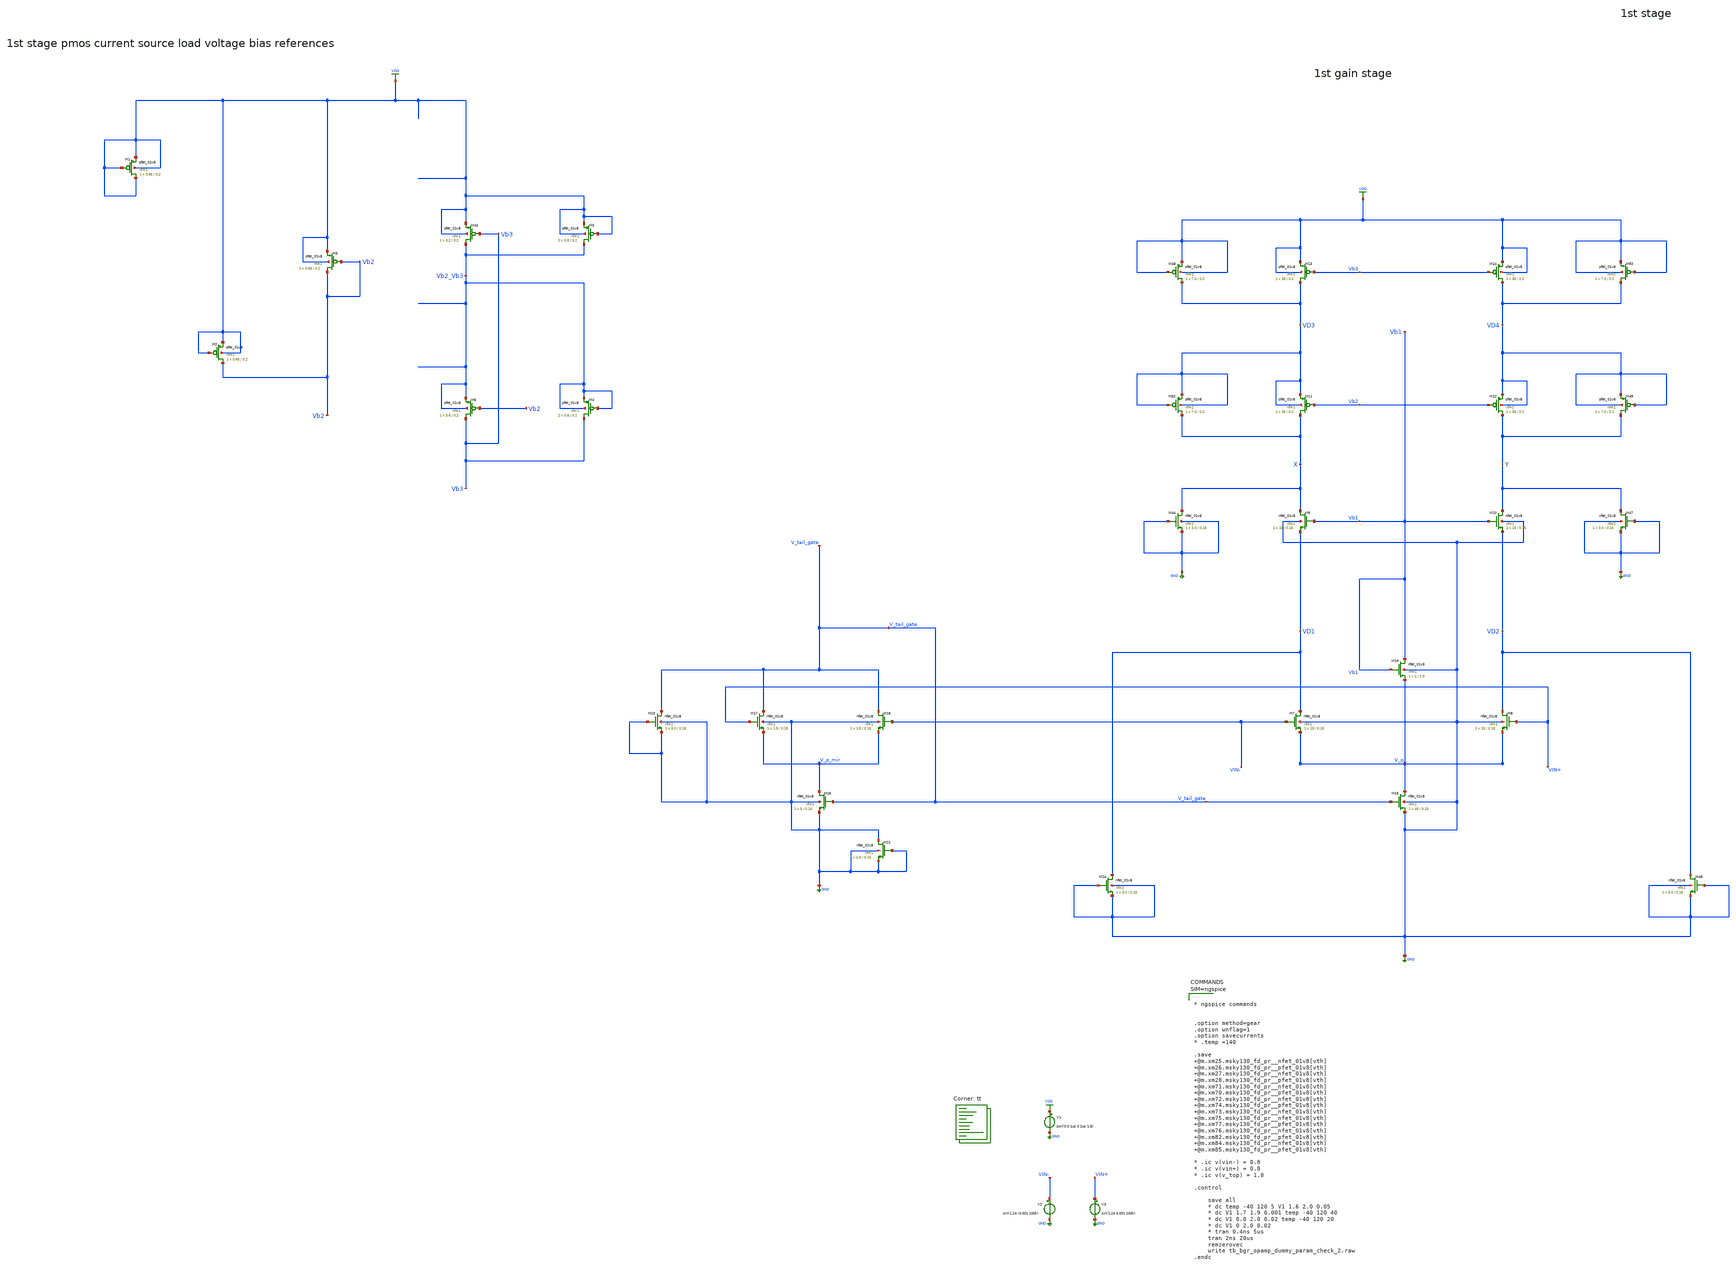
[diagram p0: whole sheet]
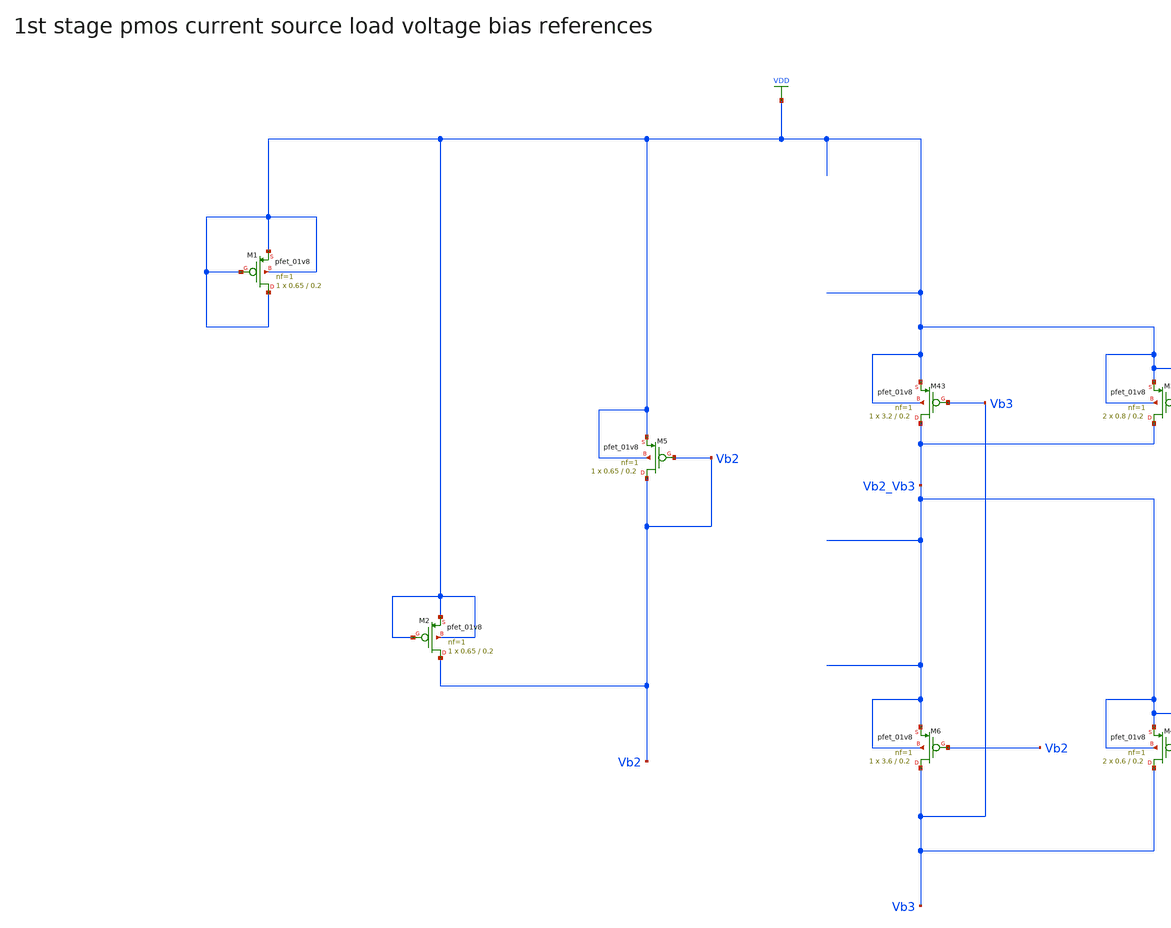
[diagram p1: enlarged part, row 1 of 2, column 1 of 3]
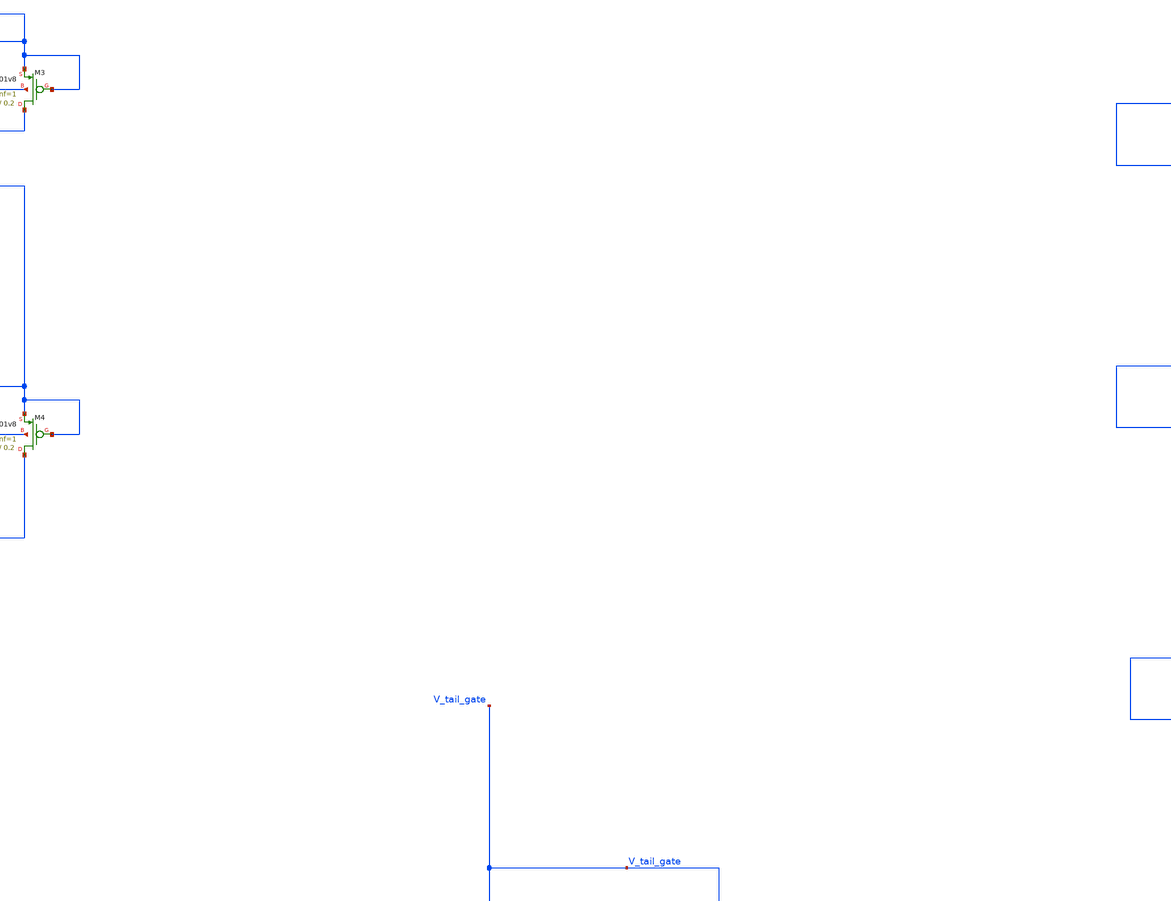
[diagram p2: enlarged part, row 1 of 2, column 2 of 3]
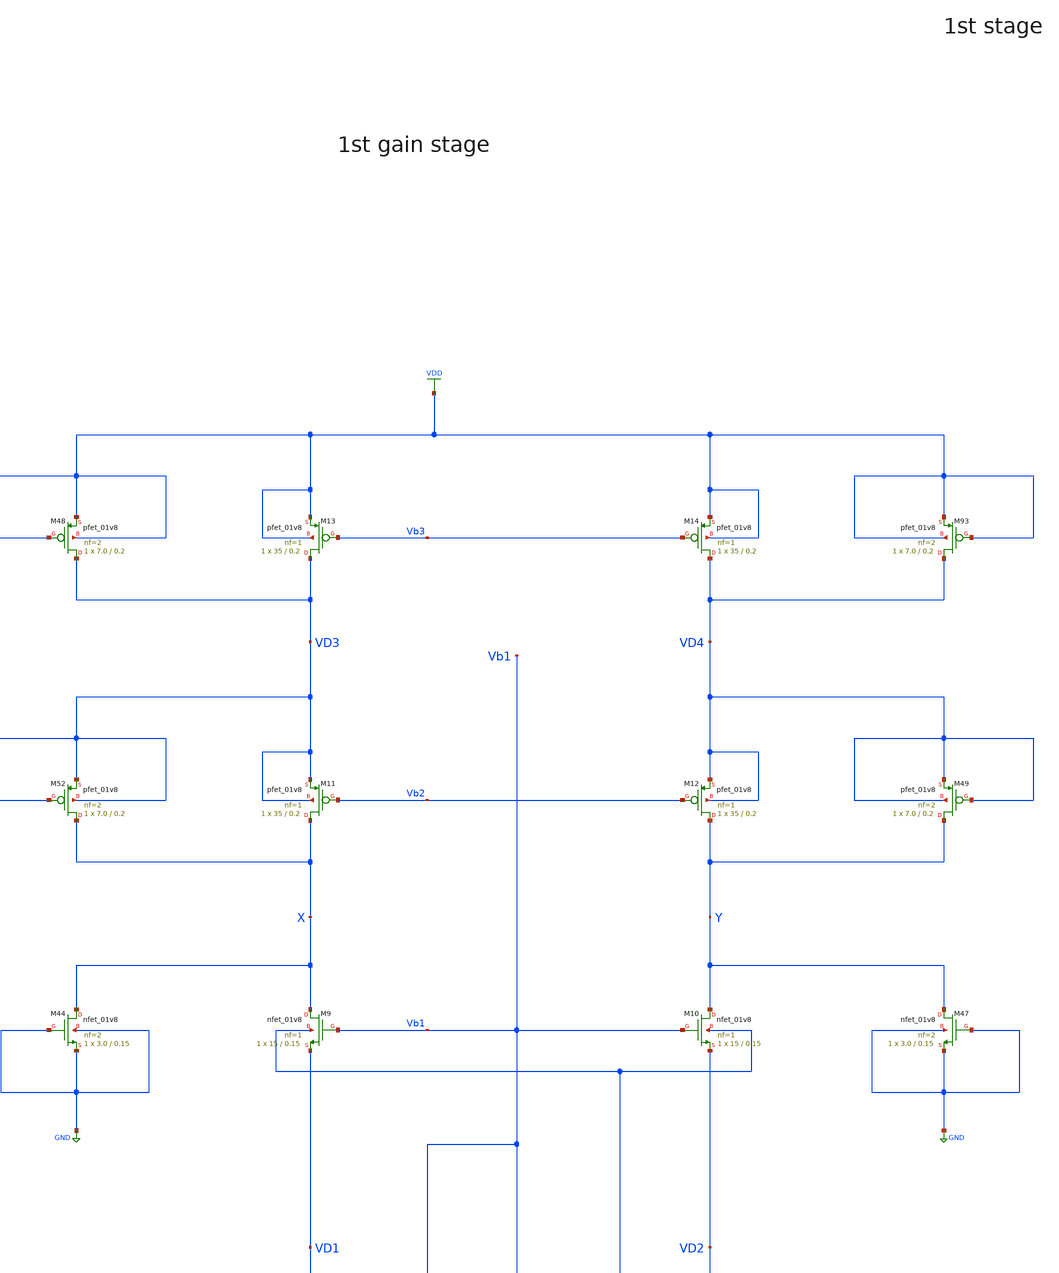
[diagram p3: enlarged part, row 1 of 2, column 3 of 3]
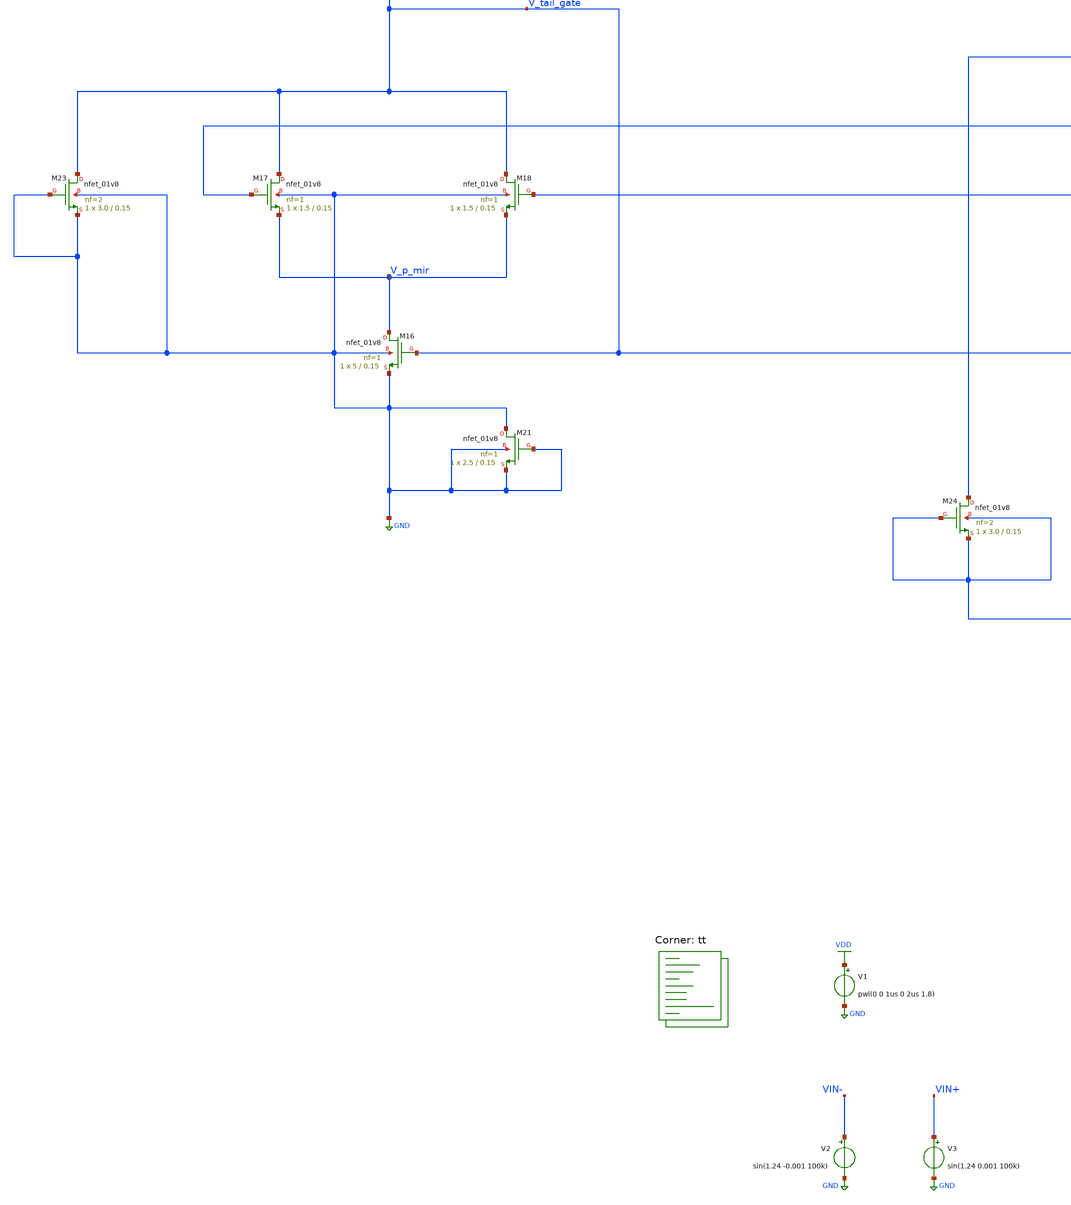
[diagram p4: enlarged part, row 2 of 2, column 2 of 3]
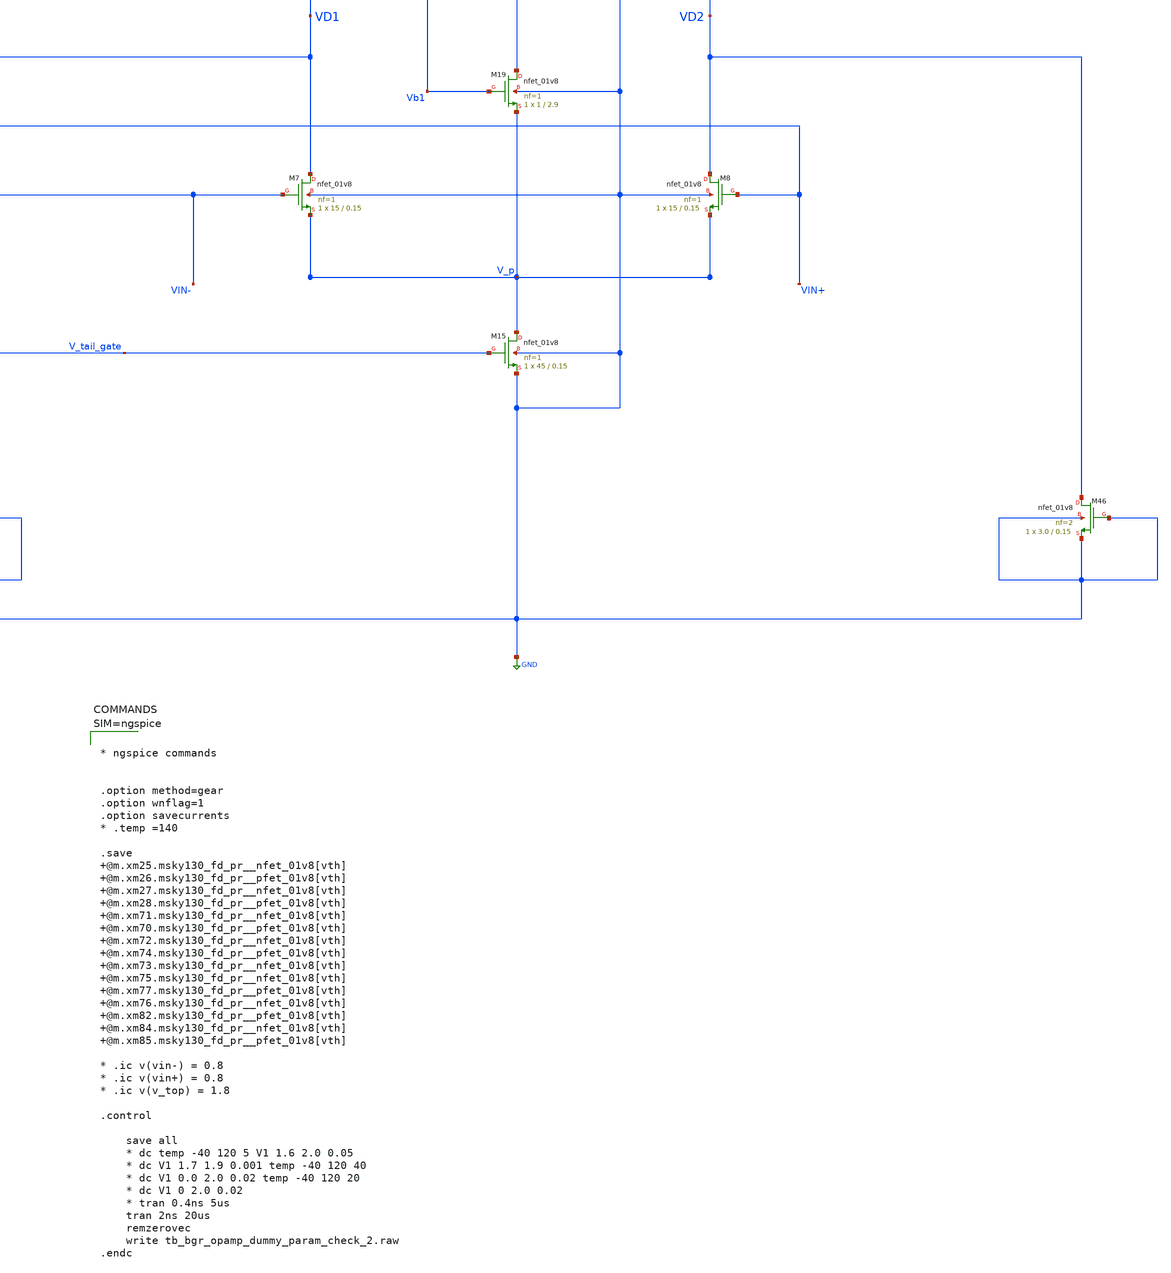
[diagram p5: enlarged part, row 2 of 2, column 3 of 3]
** sch_path: projects/ASU/EEE572/schematic/tb_bgr_opamp_dummy_param_check_2.sch
**.subckt tb_bgr_opamp_dummy_param_check_2
V1 VDD GND pwl(0 0 1us 0 2us 1.8)
XM7 VD1 VIN- V_p GND sky130_fd_pr__nfet_01v8 L=0.15 W=15 nf=1 ad='int((nf+1)/2) * W/nf * 0.29' as='int((nf+2)/2) * W/nf * 0.29'
+ pd='2*int((nf+1)/2) * (W/nf + 0.29)' ps='2*int((nf+2)/2) * (W/nf + 0.29)' nrd='0.29 / W' nrs='0.29 / W'
+ sa=0 sb=0 sd=0 mult=1 m=1
XM8 VD2 VIN+ V_p GND sky130_fd_pr__nfet_01v8 L=0.15 W=15 nf=1 ad='int((nf+1)/2) * W/nf * 0.29' as='int((nf+2)/2) * W/nf * 0.29'
+ pd='2*int((nf+1)/2) * (W/nf + 0.29)' ps='2*int((nf+2)/2) * (W/nf + 0.29)' nrd='0.29 / W' nrs='0.29 / W'
+ sa=0 sb=0 sd=0 mult=1 m=1
XM9 X Vb1 VD1 GND sky130_fd_pr__nfet_01v8 L=0.15 W=15 nf=1 ad='int((nf+1)/2) * W/nf * 0.29' as='int((nf+2)/2) * W/nf * 0.29'
+ pd='2*int((nf+1)/2) * (W/nf + 0.29)' ps='2*int((nf+2)/2) * (W/nf + 0.29)' nrd='0.29 / W' nrs='0.29 / W'
+ sa=0 sb=0 sd=0 mult=1 m=1
XM10 Y Vb1 VD2 GND sky130_fd_pr__nfet_01v8 L=0.15 W=15 nf=1 ad='int((nf+1)/2) * W/nf * 0.29' as='int((nf+2)/2) * W/nf * 0.29'
+ pd='2*int((nf+1)/2) * (W/nf + 0.29)' ps='2*int((nf+2)/2) * (W/nf + 0.29)' nrd='0.29 / W' nrs='0.29 / W'
+ sa=0 sb=0 sd=0 mult=1 m=1
XM11 X Vb2 VD3 VD3 sky130_fd_pr__pfet_01v8 L=0.2 W=35 nf=1 ad='int((nf+1)/2) * W/nf * 0.29' as='int((nf+2)/2) * W/nf * 0.29'
+ pd='2*int((nf+1)/2) * (W/nf + 0.29)' ps='2*int((nf+2)/2) * (W/nf + 0.29)' nrd='0.29 / W' nrs='0.29 / W'
+ sa=0 sb=0 sd=0 mult=1 m=1
XM12 Y Vb2 VD4 VD4 sky130_fd_pr__pfet_01v8 L=0.2 W=35 nf=1 ad='int((nf+1)/2) * W/nf * 0.29' as='int((nf+2)/2) * W/nf * 0.29'
+ pd='2*int((nf+1)/2) * (W/nf + 0.29)' ps='2*int((nf+2)/2) * (W/nf + 0.29)' nrd='0.29 / W' nrs='0.29 / W'
+ sa=0 sb=0 sd=0 mult=1 m=1
XM13 VD3 Vb3 VDD VDD sky130_fd_pr__pfet_01v8 L=0.2 W=35 nf=1 ad='int((nf+1)/2) * W/nf * 0.29' as='int((nf+2)/2) * W/nf * 0.29'
+ pd='2*int((nf+1)/2) * (W/nf + 0.29)' ps='2*int((nf+2)/2) * (W/nf + 0.29)' nrd='0.29 / W' nrs='0.29 / W'
+ sa=0 sb=0 sd=0 mult=1 m=1
XM14 VD4 Vb3 VDD VDD sky130_fd_pr__pfet_01v8 L=0.2 W=35 nf=1 ad='int((nf+1)/2) * W/nf * 0.29' as='int((nf+2)/2) * W/nf * 0.29'
+ pd='2*int((nf+1)/2) * (W/nf + 0.29)' ps='2*int((nf+2)/2) * (W/nf + 0.29)' nrd='0.29 / W' nrs='0.29 / W'
+ sa=0 sb=0 sd=0 mult=1 m=1
XM15 V_p V_tail_gate GND GND sky130_fd_pr__nfet_01v8 L=0.15 W=45 nf=1 ad='int((nf+1)/2) * W/nf * 0.29'
+ as='int((nf+2)/2) * W/nf * 0.29' pd='2*int((nf+1)/2) * (W/nf + 0.29)' ps='2*int((nf+2)/2) * (W/nf + 0.29)'
+ nrd='0.29 / W' nrs='0.29 / W' sa=0 sb=0 sd=0 mult=1 m=1
XM16 V_p_mir V_tail_gate GND GND sky130_fd_pr__nfet_01v8 L=0.15 W=5 nf=1 ad='int((nf+1)/2) * W/nf * 0.29'
+ as='int((nf+2)/2) * W/nf * 0.29' pd='2*int((nf+1)/2) * (W/nf + 0.29)' ps='2*int((nf+2)/2) * (W/nf + 0.29)'
+ nrd='0.29 / W' nrs='0.29 / W' sa=0 sb=0 sd=0 mult=1 m=1
XM17 V_tail_gate VIN+ V_p_mir GND sky130_fd_pr__nfet_01v8 L=0.15 W=1.5 nf=1 ad='int((nf+1)/2) * W/nf * 0.29'
+ as='int((nf+2)/2) * W/nf * 0.29' pd='2*int((nf+1)/2) * (W/nf + 0.29)' ps='2*int((nf+2)/2) * (W/nf + 0.29)'
+ nrd='0.29 / W' nrs='0.29 / W' sa=0 sb=0 sd=0 mult=1 m=1
XM18 V_tail_gate VIN- V_p_mir GND sky130_fd_pr__nfet_01v8 L=0.15 W=1.5 nf=1 ad='int((nf+1)/2) * W/nf * 0.29'
+ as='int((nf+2)/2) * W/nf * 0.29' pd='2*int((nf+1)/2) * (W/nf + 0.29)' ps='2*int((nf+2)/2) * (W/nf + 0.29)'
+ nrd='0.29 / W' nrs='0.29 / W' sa=0 sb=0 sd=0 mult=1 m=1
XM19 Vb1 Vb1 V_p GND sky130_fd_pr__nfet_01v8 L=2.9 W=1 nf=1 ad='int((nf+1)/2) * W/nf * 0.29' as='int((nf+2)/2) * W/nf * 0.29'
+ pd='2*int((nf+1)/2) * (W/nf + 0.29)' ps='2*int((nf+2)/2) * (W/nf + 0.29)' nrd='0.29 / W' nrs='0.29 / W'
+ sa=0 sb=0 sd=0 mult=1 m=1
XM5 Vb2 Vb2 VDD VDD sky130_fd_pr__pfet_01v8 L=0.2 W=0.65 nf=1 ad='int((nf+1)/2) * W/nf * 0.29' as='int((nf+2)/2) * W/nf * 0.29'
+ pd='2*int((nf+1)/2) * (W/nf + 0.29)' ps='2*int((nf+2)/2) * (W/nf + 0.29)' nrd='0.29 / W' nrs='0.29 / W'
+ sa=0 sb=0 sd=0 mult=1 m=1
XM6 Vb3 Vb2 Vb2_Vb3 Vb2_Vb3 sky130_fd_pr__pfet_01v8 L=0.2 W=3.6 nf=1 ad='int((nf+1)/2) * W/nf * 0.29'
+ as='int((nf+2)/2) * W/nf * 0.29' pd='2*int((nf+1)/2) * (W/nf + 0.29)' ps='2*int((nf+2)/2) * (W/nf + 0.29)'
+ nrd='0.29 / W' nrs='0.29 / W' sa=0 sb=0 sd=0 mult=1 m=1
XM43 Vb2_Vb3 Vb3 VDD VDD sky130_fd_pr__pfet_01v8 L=0.2 W=3.2 nf=1 ad='int((nf+1)/2) * W/nf * 0.29' as='int((nf+2)/2) * W/nf * 0.29'
+ pd='2*int((nf+1)/2) * (W/nf + 0.29)' ps='2*int((nf+2)/2) * (W/nf + 0.29)' nrd='0.29 / W' nrs='0.29 / W'
+ sa=0 sb=0 sd=0 mult=1 m=1
XM1 VDD VDD VDD VDD sky130_fd_pr__pfet_01v8 L=0.2 W=0.65 nf=1 ad='int((nf+1)/2) * W/nf * 0.29' as='int((nf+2)/2) * W/nf * 0.29'
+ pd='2*int((nf+1)/2) * (W/nf + 0.29)' ps='2*int((nf+2)/2) * (W/nf + 0.29)' nrd='0.29 / W' nrs='0.29 / W'
+ sa=0 sb=0 sd=0 mult=1 m=1
XM2 Vb2 VDD VDD VDD sky130_fd_pr__pfet_01v8 L=0.2 W=0.65 nf=1 ad='int((nf+1)/2) * W/nf * 0.29' as='int((nf+2)/2) * W/nf * 0.29'
+ pd='2*int((nf+1)/2) * (W/nf + 0.29)' ps='2*int((nf+2)/2) * (W/nf + 0.29)' nrd='0.29 / W' nrs='0.29 / W'
+ sa=0 sb=0 sd=0 mult=1 m=1
XM4 Vb3 Vb2_Vb3 Vb2_Vb3 Vb2_Vb3 sky130_fd_pr__pfet_01v8 L=0.2 W=0.6 nf=1 ad='int((nf+1)/2) * W/nf * 0.29'
+ as='int((nf+2)/2) * W/nf * 0.29' pd='2*int((nf+1)/2) * (W/nf + 0.29)' ps='2*int((nf+2)/2) * (W/nf + 0.29)'
+ nrd='0.29 / W' nrs='0.29 / W' sa=0 sb=0 sd=0 mult=2 m=2
XM21 GND GND GND GND sky130_fd_pr__nfet_01v8 L=0.15 W=2.5 nf=1 ad='int((nf+1)/2) * W/nf * 0.29' as='int((nf+2)/2) * W/nf * 0.29'
+ pd='2*int((nf+1)/2) * (W/nf + 0.29)' ps='2*int((nf+2)/2) * (W/nf + 0.29)' nrd='0.29 / W' nrs='0.29 / W'
+ sa=0 sb=0 sd=0 mult=1 m=1
XM23 V_tail_gate GND GND GND sky130_fd_pr__nfet_01v8 L=0.15 W=3.0 nf=2 ad='int((nf+1)/2) * W/nf * 0.29'
+ as='int((nf+2)/2) * W/nf * 0.29' pd='2*int((nf+1)/2) * (W/nf + 0.29)' ps='2*int((nf+2)/2) * (W/nf + 0.29)'
+ nrd='0.29 / W' nrs='0.29 / W' sa=0 sb=0 sd=0 mult=1 m=1
XM24 VD1 GND GND GND sky130_fd_pr__nfet_01v8 L=0.15 W=3.0 nf=2 ad='int((nf+1)/2) * W/nf * 0.29' as='int((nf+2)/2) * W/nf * 0.29'
+ pd='2*int((nf+1)/2) * (W/nf + 0.29)' ps='2*int((nf+2)/2) * (W/nf + 0.29)' nrd='0.29 / W' nrs='0.29 / W'
+ sa=0 sb=0 sd=0 mult=1 m=1
XM46 VD2 GND GND GND sky130_fd_pr__nfet_01v8 L=0.15 W=3.0 nf=2 ad='int((nf+1)/2) * W/nf * 0.29' as='int((nf+2)/2) * W/nf * 0.29'
+ pd='2*int((nf+1)/2) * (W/nf + 0.29)' ps='2*int((nf+2)/2) * (W/nf + 0.29)' nrd='0.29 / W' nrs='0.29 / W'
+ sa=0 sb=0 sd=0 mult=1 m=1
XM47 Y GND GND GND sky130_fd_pr__nfet_01v8 L=0.15 W=3.0 nf=2 ad='int((nf+1)/2) * W/nf * 0.29' as='int((nf+2)/2) * W/nf * 0.29'
+ pd='2*int((nf+1)/2) * (W/nf + 0.29)' ps='2*int((nf+2)/2) * (W/nf + 0.29)' nrd='0.29 / W' nrs='0.29 / W'
+ sa=0 sb=0 sd=0 mult=1 m=1
XM48 VD3 VDD VDD VDD sky130_fd_pr__pfet_01v8 L=0.2 W=7.0 nf=2 ad='int((nf+1)/2) * W/nf * 0.29' as='int((nf+2)/2) * W/nf * 0.29'
+ pd='2*int((nf+1)/2) * (W/nf + 0.29)' ps='2*int((nf+2)/2) * (W/nf + 0.29)' nrd='0.29 / W' nrs='0.29 / W'
+ sa=0 sb=0 sd=0 mult=1 m=1
XM49 Y VD4 VD4 VD4 sky130_fd_pr__pfet_01v8 L=0.2 W=7.0 nf=2 ad='int((nf+1)/2) * W/nf * 0.29' as='int((nf+2)/2) * W/nf * 0.29'
+ pd='2*int((nf+1)/2) * (W/nf + 0.29)' ps='2*int((nf+2)/2) * (W/nf + 0.29)' nrd='0.29 / W' nrs='0.29 / W'
+ sa=0 sb=0 sd=0 mult=1 m=1
XM52 X VD3 VD3 VD3 sky130_fd_pr__pfet_01v8 L=0.2 W=7.0 nf=2 ad='int((nf+1)/2) * W/nf * 0.29' as='int((nf+2)/2) * W/nf * 0.29'
+ pd='2*int((nf+1)/2) * (W/nf + 0.29)' ps='2*int((nf+2)/2) * (W/nf + 0.29)' nrd='0.29 / W' nrs='0.29 / W'
+ sa=0 sb=0 sd=0 mult=1 m=1
XM44 X GND GND GND sky130_fd_pr__nfet_01v8 L=0.15 W=3.0 nf=2 ad='int((nf+1)/2) * W/nf * 0.29' as='int((nf+2)/2) * W/nf * 0.29'
+ pd='2*int((nf+1)/2) * (W/nf + 0.29)' ps='2*int((nf+2)/2) * (W/nf + 0.29)' nrd='0.29 / W' nrs='0.29 / W'
+ sa=0 sb=0 sd=0 mult=1 m=1
XM93 VD4 VDD VDD VDD sky130_fd_pr__pfet_01v8 L=0.2 W=7.0 nf=2 ad='int((nf+1)/2) * W/nf * 0.29' as='int((nf+2)/2) * W/nf * 0.29'
+ pd='2*int((nf+1)/2) * (W/nf + 0.29)' ps='2*int((nf+2)/2) * (W/nf + 0.29)' nrd='0.29 / W' nrs='0.29 / W'
+ sa=0 sb=0 sd=0 mult=1 m=1
V2 VIN- GND sin(1.24 -0.001 100k)
V3 VIN+ GND sin(1.24 0.001 100k)
XM3 Vb2_Vb3 VDD VDD VDD sky130_fd_pr__pfet_01v8 L=0.2 W=0.8 nf=1 ad='int((nf+1)/2) * W/nf * 0.29' as='int((nf+2)/2) * W/nf * 0.29'
+ pd='2*int((nf+1)/2) * (W/nf + 0.29)' ps='2*int((nf+2)/2) * (W/nf + 0.29)' nrd='0.29 / W' nrs='0.29 / W'
+ sa=0 sb=0 sd=0 mult=2 m=2
**** begin user architecture code
.lib $::SKYWATER_MODELS/sky130.lib.spice tt



* ngspice commands


.option method=gear
.option wnflag=1
.option savecurrents
* .temp =140

.save @m.xm25.msky130_fd_pr__nfet_01v8[vth] @m.xm26.msky130_fd_pr__pfet_01v8[vth] @m.xm27.msky130_fd_pr__nfet_01v8[vth] @m.xm28.msky130_fd_pr__pfet_01v8[vth] @m.xm71.msky130_fd_pr__nfet_01v8[vth] @m.xm70.msky130_fd_pr__pfet_01v8[vth] @m.xm72.msky130_fd_pr__nfet_01v8[vth] @m.xm74.msky130_fd_pr__pfet_01v8[vth] @m.xm73.msky130_fd_pr__nfet_01v8[vth] @m.xm75.msky130_fd_pr__nfet_01v8[vth] @m.xm77.msky130_fd_pr__pfet_01v8[vth] @m.xm76.msky130_fd_pr__nfet_01v8[vth] @m.xm82.msky130_fd_pr__pfet_01v8[vth] @m.xm84.msky130_fd_pr__nfet_01v8[vth] @m.xm85.msky130_fd_pr__pfet_01v8[vth]

* .ic v(vin-) = 0.8
* .ic v(vin+) = 0.8
* .ic v(v_top) = 1.8

.control

    save all
    * dc temp -40 120 5 V1 1.6 2.0 0.05
    * dc V1 1.7 1.9 0.001 temp -40 120 40
    * dc V1 0.0 2.0 0.02 temp -40 120 20
    * dc V1 0 2.0 0.02
    * tran 0.4ns 5us
    tran 2ns 20us
    remzerovec
    write tb_bgr_opamp_dummy_param_check_2.raw
.endc




**** end user architecture code
**.ends
.GLOBAL GND
.GLOBAL VDD
.end
